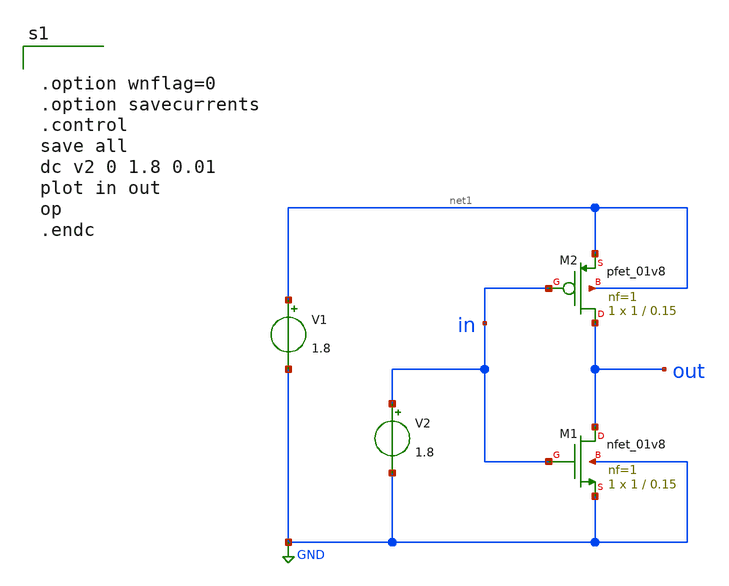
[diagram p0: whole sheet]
** sch_path: inverter_tb.sch
**.subckt inverter_tb
XM1 out in GND GND sky130_fd_pr__nfet_01v8 L=0.15 W=1 nf=1 ad='int((nf+1)/2) * W/nf * 0.29' as='int((nf+2)/2) * W/nf * 0.29'
+ pd='2*int((nf+1)/2) * (W/nf + 0.29)' ps='2*int((nf+2)/2) * (W/nf + 0.29)' nrd='0.29 / W' nrs='0.29 / W'
+ sa=0 sb=0 sd=0 mult=1 m=1
XM2 out in net1 net1 sky130_fd_pr__pfet_01v8 L=0.15 W=1 nf=1 ad='int((nf+1)/2) * W/nf * 0.29' as='int((nf+2)/2) * W/nf * 0.29'
+ pd='2*int((nf+1)/2) * (W/nf + 0.29)' ps='2*int((nf+2)/2) * (W/nf + 0.29)' nrd='0.29 / W' nrs='0.29 / W'
+ sa=0 sb=0 sd=0 mult=1 m=1
V1 net1 GND 1.8
V2 in GND 1.8
**** begin user architecture code

** opencircuitdesign pdks install
.lib $::SKYWATER_MODELS/sky130.lib.spice tt




.option wnflag=0
.option savecurrents
.control
save all
dc v2 0 1.8 0.01
plot in out
op
.endc


**** end user architecture code
**.ends
.GLOBAL GND
.end
